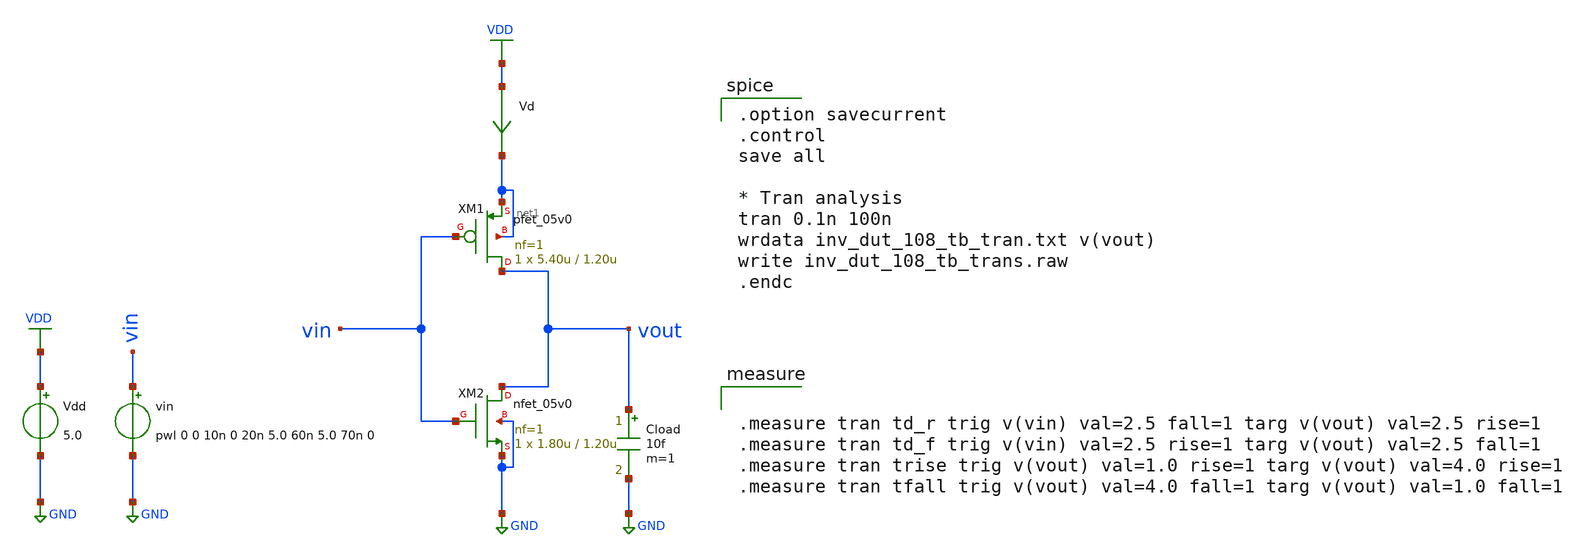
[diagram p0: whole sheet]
** sch_path: inv_dut_108_tb_trans.sch
**.subckt inv_dut_108_tb_trans
Vdd VDD GND 5.0
vin vin GND pwl 0 0 10n 0 20n 5.0 60n 5.0 70n 0
Vd VDD net1 0
.save i(vd)
Cload vout GND 10f m=1
XM1 vout vin net1 net1 pfet_05v0 L=1.20u W=5.40u nf=1 ad='int((nf+1)/2) * W/nf * 0.18u' as='int((nf+2)/2) * W/nf * 0.18u'
+ pd='2*int((nf+1)/2) * (W/nf + 0.18u)' ps='2*int((nf+2)/2) * (W/nf + 0.18u)' nrd='0.18u / W' nrs='0.18u / W'
+ sa=0 sb=0 sd=0 m=1
XM2 vout vin GND GND nfet_05v0 L=1.20u W=1.80u nf=1 ad='int((nf+1)/2) * W/nf * 0.18u' as='int((nf+2)/2) * W/nf * 0.18u'
+ pd='2*int((nf+1)/2) * (W/nf + 0.18u)' ps='2*int((nf+2)/2) * (W/nf + 0.18u)' nrd='0.18u / W' nrs='0.18u / W'
+ sa=0 sb=0 sd=0 m=1
**** begin user architecture code

.option savecurrent
.control
save all

* Tran analysis
tran 0.1n 100n
wrdata inv_dut_108_tb_tran.txt v(vout)
write inv_dut_108_tb_trans.raw
.endc



.measure tran td_r trig v(vin) val=2.5 fall=1 targ v(vout) val=2.5 rise=1
.measure tran td_f trig v(vin) val=2.5 rise=1 targ v(vout) val=2.5 fall=1
.measure tran trise trig v(vout) val=1.0 rise=1 targ v(vout) val=4.0 rise=1
.measure tran tfall trig v(vout) val=4.0 fall=1 targ v(vout) val=1.0 fall=1



.include $::180MCU_MODELS/design.ngspice
.lib $::180MCU_MODELS/sm141064.ngspice typical
.lib $::180MCU_MODELS/sm141064.ngspice res_typical
.lib $::180MCU_MODELS/sm141064.ngspice moscap_typical
.lib $::180MCU_MODELS/sm141064.ngspice diode_typical

**** end user architecture code
**.ends
.GLOBAL VDD
.GLOBAL GND
.end
